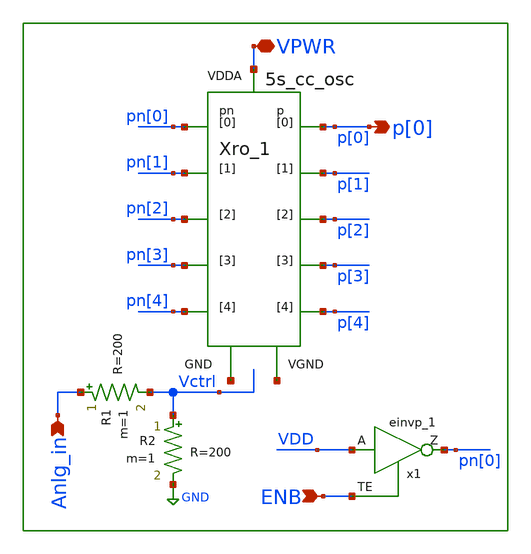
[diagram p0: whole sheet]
** sch_path: xschem/lib/ALib_VCO.sch
**.subckt ALib_VCO Anlg_in VPWR p[0] ENB
*.ipin Anlg_in
*.iopin VPWR
*.opin p[0]
*.ipin ENB
x1 VDD ENB GND GND VDD VDD pn[0] sky130_fd_sc_hd__einvp_1
R2 Vctrl GND R=200 m=1
R1 Anlg_in Vctrl R=200 m=1
Xro_1 net1 VPWR p[0] p[1] p[2] p[3] p[4] pn[0] pn[1] pn[2] pn[3] pn[4] net2 5s_cc_osc
**.ends
.GLOBAL GND
.end
